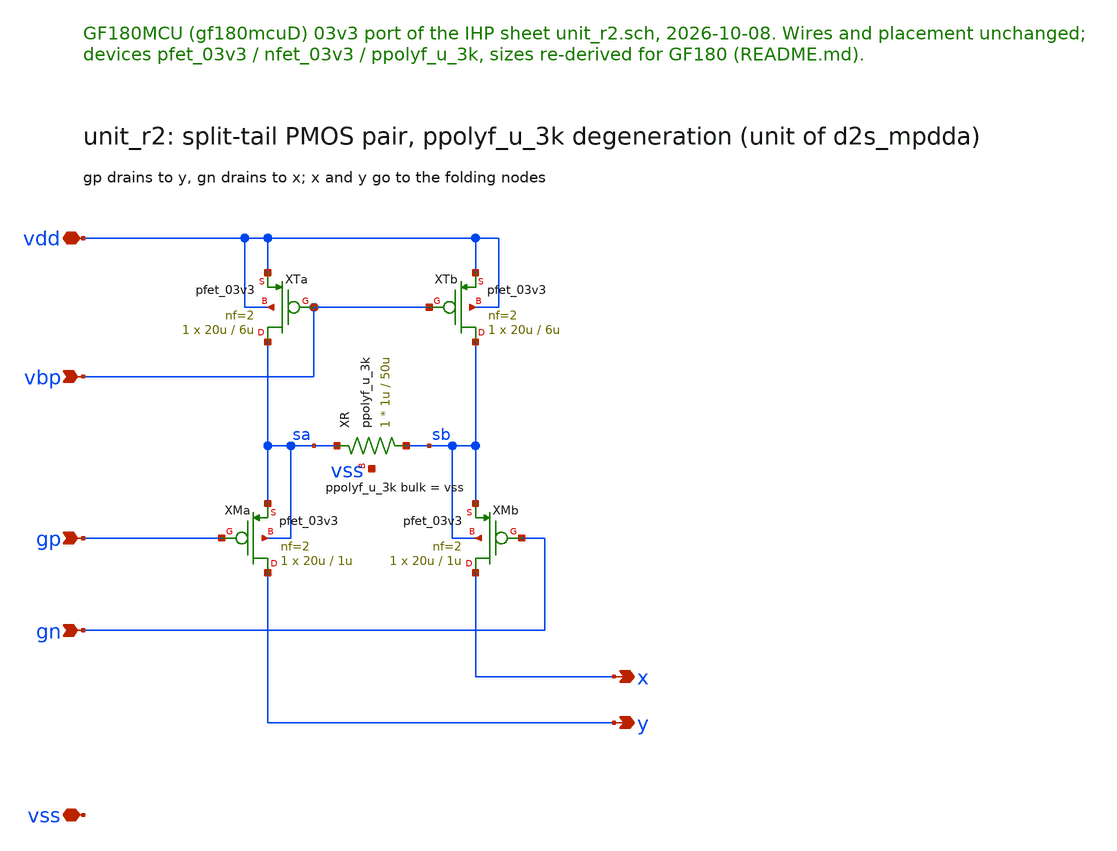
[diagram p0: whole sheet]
** sch_path: macros/ClassABDriver/schematic/xschem/ClassABUnitR.sch
**.subckt ClassABUnitR x y gp gn vdd vss vbp
*.opin x
*.opin y
*.ipin gp
*.ipin gn
*.iopin vdd
*.iopin vss
*.ipin vbp
XTa sa vbp vdd vdd pfet_03v3 L=6u W=20u nf=2 ad='int((nf+1)/2) * W/nf * 0.18u' as='int((nf+2)/2) * W/nf * 0.18u'
+ pd='2*int((nf+1)/2) * (W/nf + 0.18u)' ps='2*int((nf+2)/2) * (W/nf + 0.18u)' nrd='0.18u / W' nrs='0.18u / W'
+ sa=0 sb=0 sd=0 m=1
XTb sb vbp vdd vdd pfet_03v3 L=6u W=20u nf=2 ad='int((nf+1)/2) * W/nf * 0.18u' as='int((nf+2)/2) * W/nf * 0.18u'
+ pd='2*int((nf+1)/2) * (W/nf + 0.18u)' ps='2*int((nf+2)/2) * (W/nf + 0.18u)' nrd='0.18u / W' nrs='0.18u / W'
+ sa=0 sb=0 sd=0 m=1
XMa y gp sa sa pfet_03v3 L=1u W=20u nf=2 ad='int((nf+1)/2) * W/nf * 0.18u' as='int((nf+2)/2) * W/nf * 0.18u'
+ pd='2*int((nf+1)/2) * (W/nf + 0.18u)' ps='2*int((nf+2)/2) * (W/nf + 0.18u)' nrd='0.18u / W' nrs='0.18u / W'
+ sa=0 sb=0 sd=0 m=1
XMb x gn sb sb pfet_03v3 L=1u W=20u nf=2 ad='int((nf+1)/2) * W/nf * 0.18u' as='int((nf+2)/2) * W/nf * 0.18u'
+ pd='2*int((nf+1)/2) * (W/nf + 0.18u)' ps='2*int((nf+2)/2) * (W/nf + 0.18u)' nrd='0.18u / W' nrs='0.18u / W'
+ sa=0 sb=0 sd=0 m=1
XR sb sa vss ppolyf_u_3k r_width=1u r_length=50u m=1
**.ends
.end
